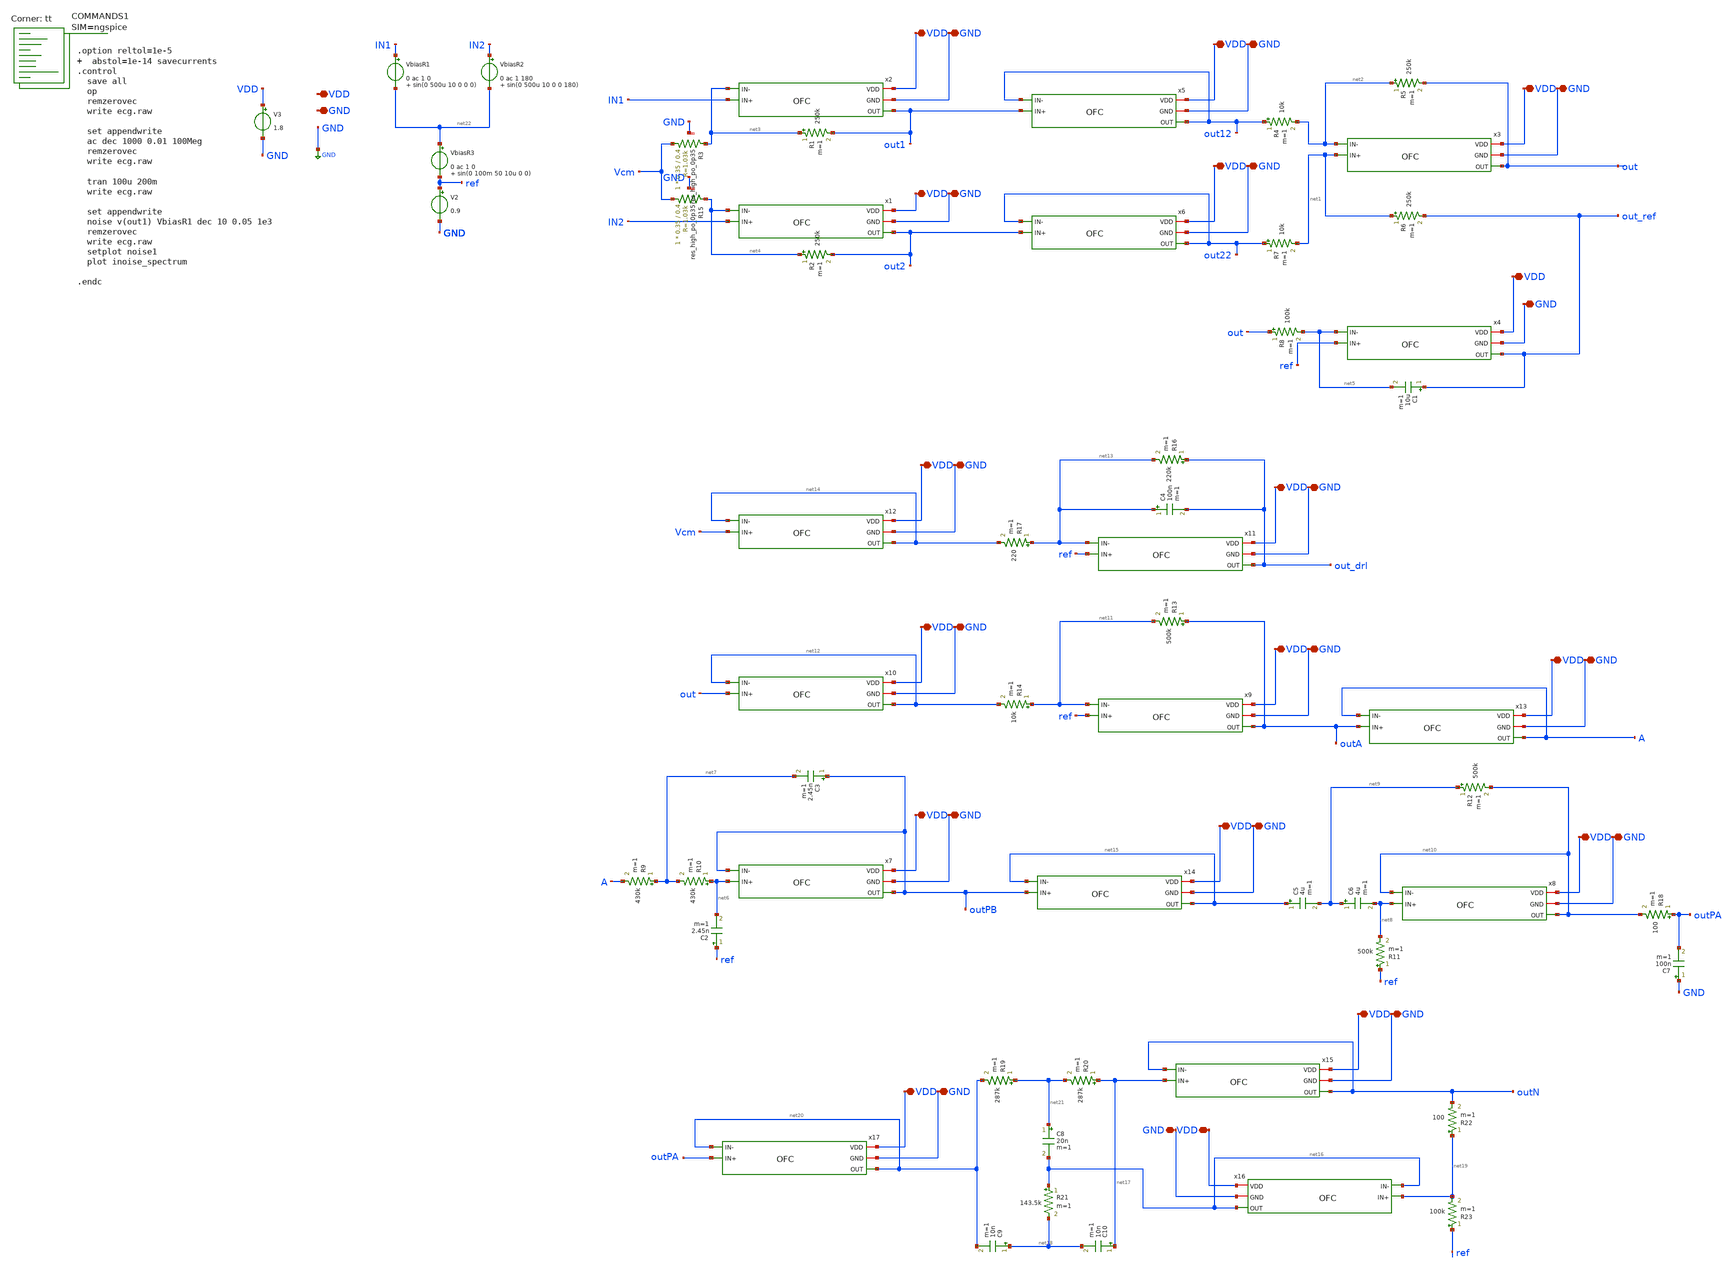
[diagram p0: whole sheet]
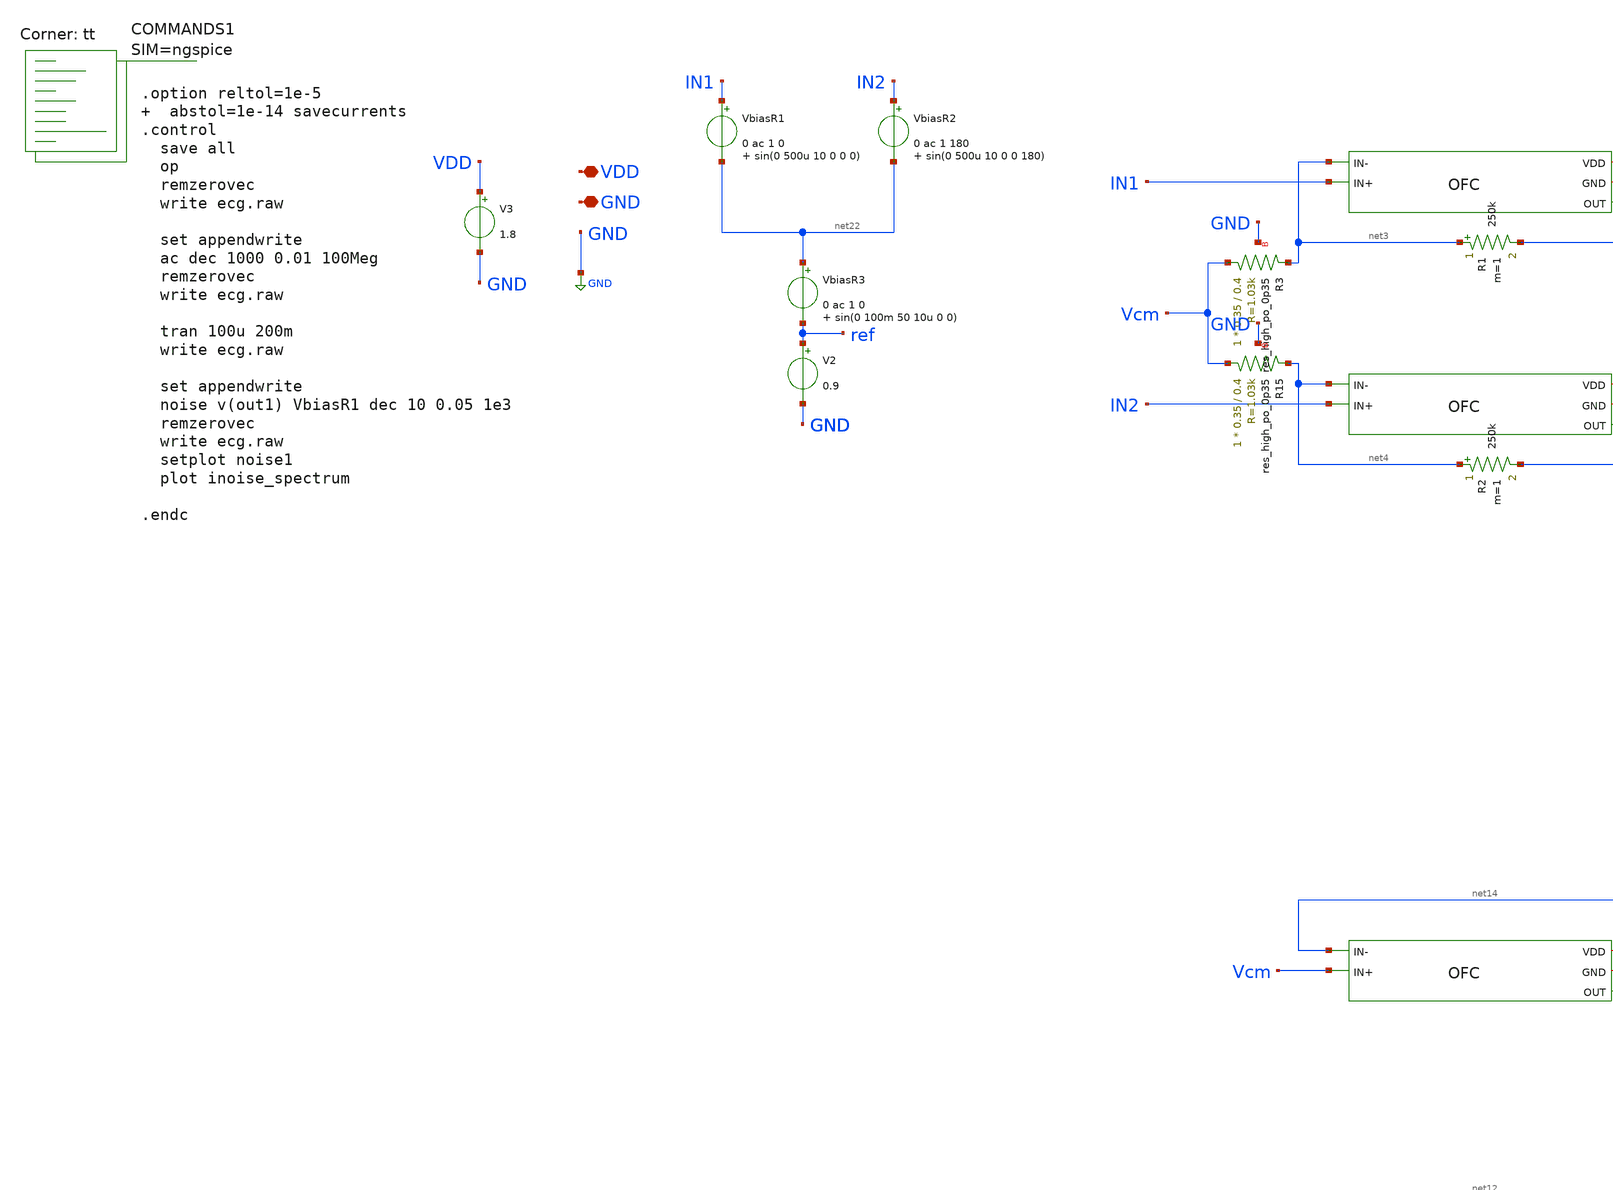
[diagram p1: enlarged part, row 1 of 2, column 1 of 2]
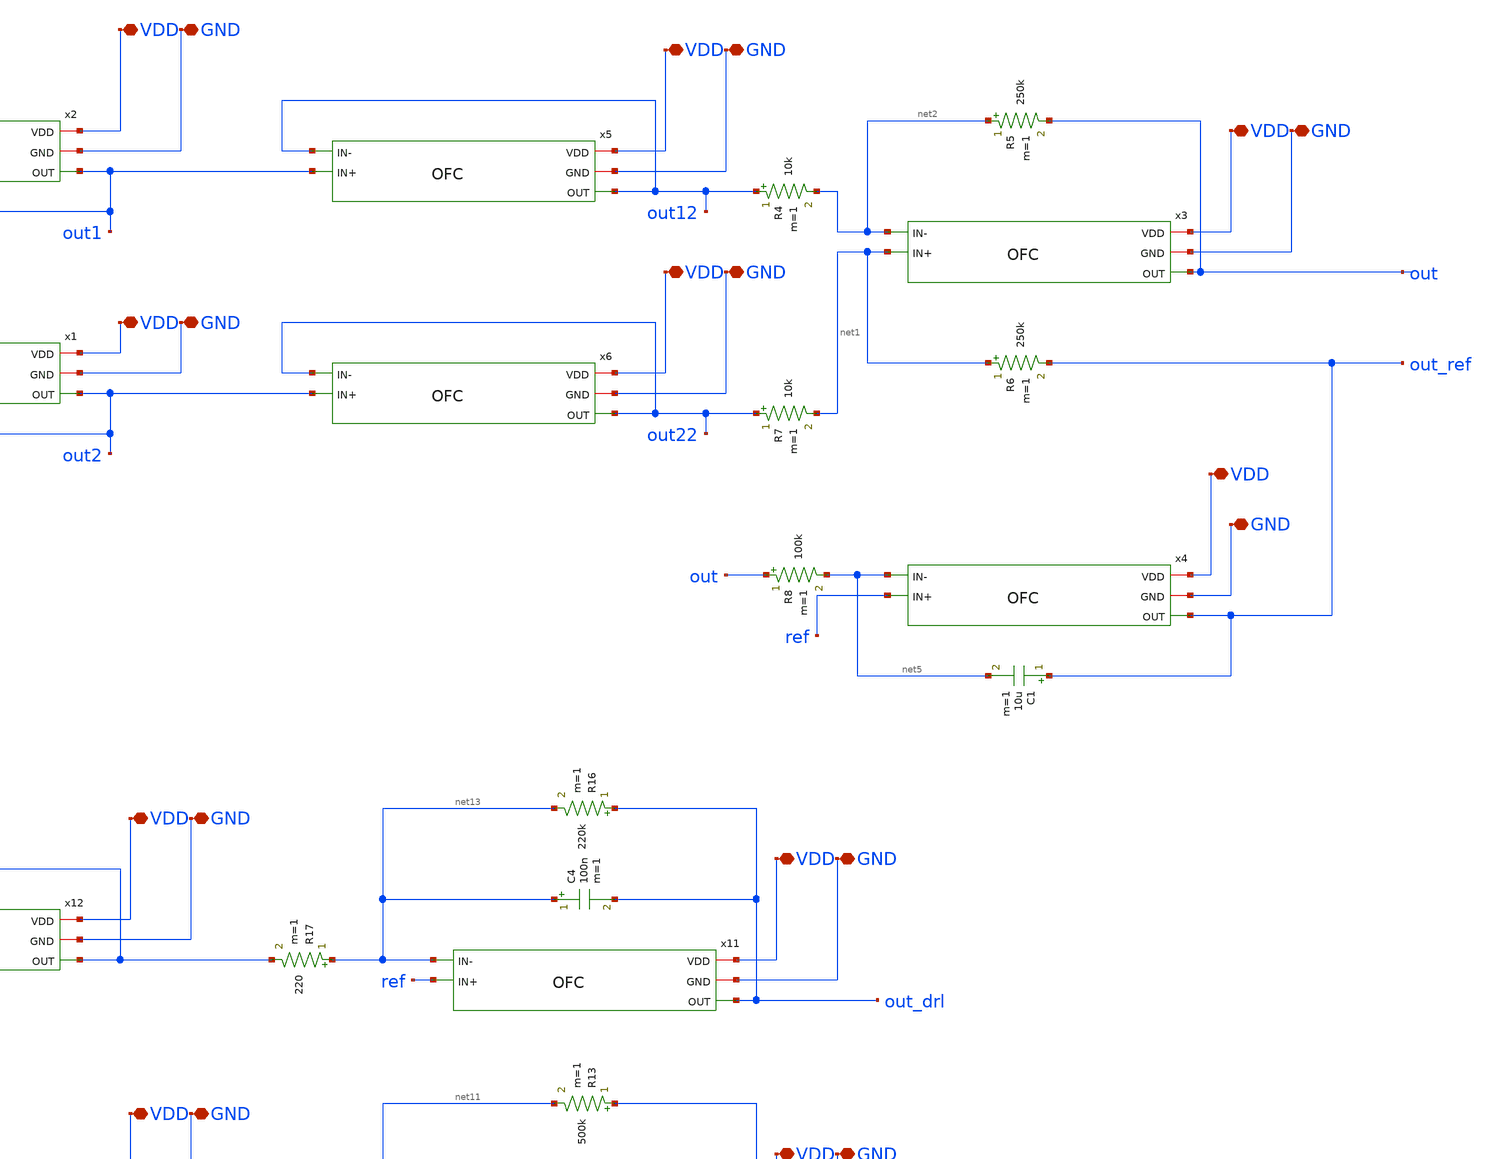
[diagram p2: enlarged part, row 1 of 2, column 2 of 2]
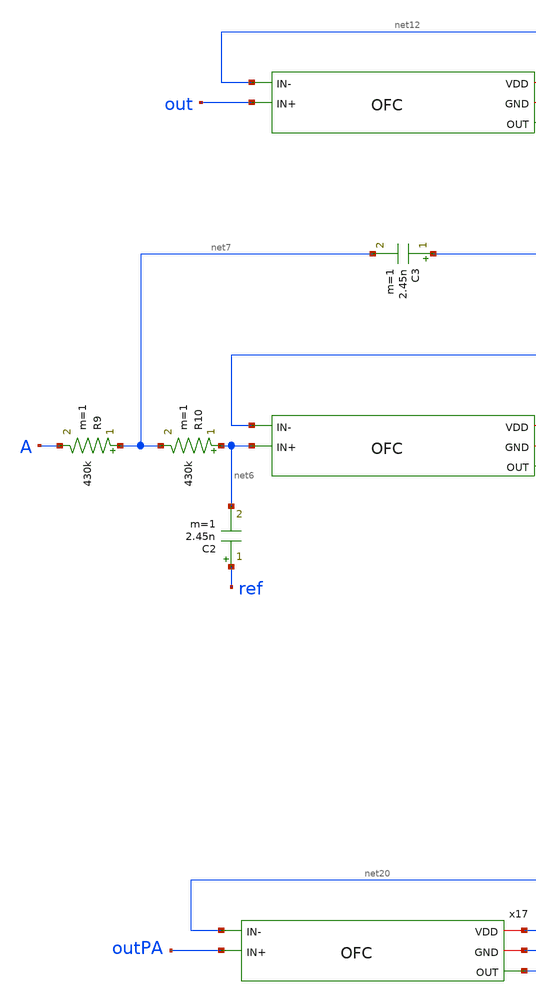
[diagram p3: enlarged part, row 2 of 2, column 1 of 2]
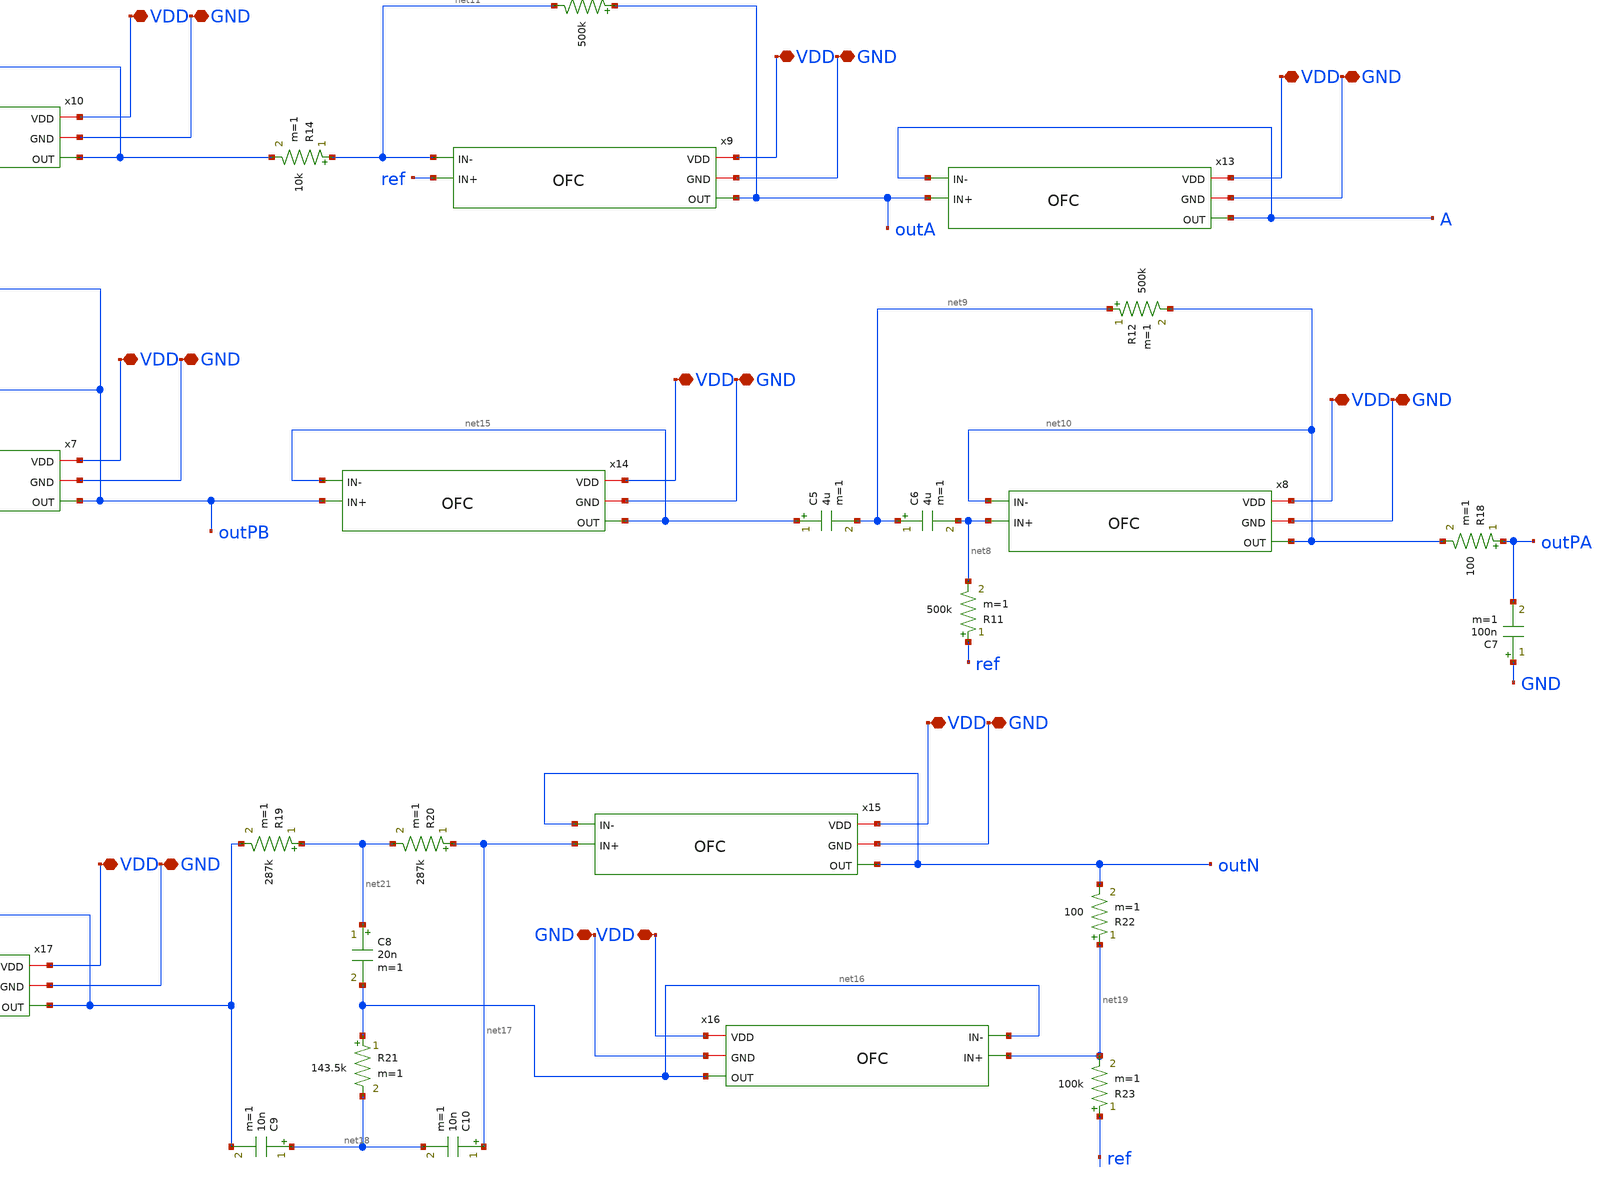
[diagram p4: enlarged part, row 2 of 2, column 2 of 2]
** sch_path: xschem/ecg.sch
**.subckt ecg VDD GND VDD VDD GND GND VDD GND VDD GND VDD GND VDD GND VDD GND VDD GND VDD GND VDD
*+ GND VDD GND VDD GND VDD GND VDD GND VDD GND VDD GND VDD GND
*.iopin VDD
*.iopin GND
*.iopin VDD
*.iopin VDD
*.iopin GND
*.iopin GND
*.iopin VDD
*.iopin GND
*.iopin VDD
*.iopin GND
*.iopin VDD
*.iopin GND
*.iopin VDD
*.iopin GND
*.iopin VDD
*.iopin GND
*.iopin VDD
*.iopin GND
*.iopin VDD
*.iopin GND
*.iopin VDD
*.iopin GND
*.iopin VDD
*.iopin GND
*.iopin VDD
*.iopin GND
*.iopin VDD
*.iopin GND
*.iopin VDD
*.iopin GND
*.iopin VDD
*.iopin GND
*.iopin VDD
*.iopin GND
*.iopin VDD
*.iopin GND
V3 VDD GND 1.8
x1 VDD GND out2 net4 IN2 OFC
x2 VDD GND out1 net3 IN1 OFC
x3 VDD GND out net2 net1 OFC
R1 net3 out1 250k m=1
R2 net4 out2 250k m=1
x4 VDD GND out_ref net5 ref OFC
R6 net1 out_ref 250k m=1
R8 out net5 100k m=1
C1 out_ref net5 10u m=1
R5 net2 out 250k m=1
x5 VDD GND out12 out12 out1 OFC
x6 VDD GND out22 out22 out2 OFC
R4 out12 net2 10k m=1
R7 out22 net1 10k m=1
x7 VDD GND outPB outPB net6 OFC
R9 net7 A 430k m=1
C2 ref net6 2.45n m=1
R10 net6 net7 430k m=1
C3 outPB net7 2.45n m=1
x8 VDD GND net10 net10 net8 OFC
R11 ref net8 500k m=1
C5 net15 net9 4u m=1
C6 net9 net8 4u m=1
x9 VDD GND outA net11 ref OFC
R13 outA net11 500k m=1
R14 net11 net12 10k m=1
x10 VDD GND net12 net12 out OFC
x11 VDD GND out_drl net13 ref OFC
R16 out_drl net13 220k m=1
R17 net13 net14 220 m=1
x12 VDD GND net14 net14 Vcm OFC
C4 net13 out_drl 100n m=1
x13 VDD GND A A outA OFC
x14 VDD GND net15 net15 outPB OFC
C7 GND outPA 100n m=1
R18 outPA net10 100 m=1
R12 net9 net10 500k m=1
XR3 Vcm net3 GND sky130_fd_pr__res_high_po_0p35 L=0.4 mult=1 m=1
XR15 Vcm net4 GND sky130_fd_pr__res_high_po_0p35 L=0.4 mult=1 m=1
x15 VDD GND outN outN net17 OFC
x16 VDD GND net16 net16 net19 OFC
R19 net21 net20 287k m=1
R20 net17 net21 287k m=1
R21 net16 net18 143.5k m=1
C8 net21 net16 20n m=1
C9 net18 net20 10n m=1
C10 net17 net18 10n m=1
R22 net19 outN 100 m=1
R23 ref net19 100k m=1
x17 VDD GND net20 net20 outPA OFC
VbiasR1 IN1 net22 0 ac 1 0 sin(0 500u 10 0 0 0)
V2 ref GND 0.9
VbiasR2 IN2 net22 0 ac 1 180 sin(0 500u 10 0 0 180)
VbiasR3 net22 ref 0 ac 1 0 sin(0 100m 50 10u 0 0)
**** begin user architecture code



.option reltol=1e-5   abstol=1e-14 savecurrents
.control
  save all
  op
  remzerovec
  write ecg.raw

  set appendwrite
  ac dec 1000 0.01 100Meg
  remzerovec
  write ecg.raw

  tran 100u 200m
  write ecg.raw

  set appendwrite
  noise v(out1) VbiasR1 dec 10 0.05 1e3
  remzerovec
  write ecg.raw
  setplot noise1
  plot inoise_spectrum

.endc



.lib $::SKYWATER_MODELS/sky130.lib.spice tt
**** end user architecture code
**.ends

* expanding   symbol:  OFC.sym # of pins=5
** sym_path: OFC.sym
** sch_path: OFC.sch
.subckt OFC VDD GND OUT IN- IN+
*.iopin VDD
*.iopin GND
*.ipin IN+
*.ipin IN-
*.opin OUT
XM11 S Vb VDD VDD sky130_fd_pr__pfet_01v8_lvt L=1 W=60 nf=2 ad='int((nf+1)/2) * W/nf * 0.29' as='int((nf+2)/2) * W/nf * 0.29'
+ pd='2*int((nf+1)/2) * (W/nf + 0.29)' ps='2*int((nf+2)/2) * (W/nf + 0.29)' nrd='0.29 / W' nrs='0.29 / W'
+ sa=0 sb=0 sd=0 mult=2 m=2
XM1 D1 IN+ S S sky130_fd_pr__pfet_01v8_lvt L=10 W=25 nf=2 ad='int((nf+1)/2) * W/nf * 0.29' as='int((nf+2)/2) * W/nf * 0.29'
+ pd='2*int((nf+1)/2) * (W/nf + 0.29)' ps='2*int((nf+2)/2) * (W/nf + 0.29)' nrd='0.29 / W' nrs='0.29 / W'
+ sa=0 sb=0 sd=0 mult=2 m=2
XM2 D2 IN- S S sky130_fd_pr__pfet_01v8_lvt L=10 W=25 nf=2 ad='int((nf+1)/2) * W/nf * 0.29' as='int((nf+2)/2) * W/nf * 0.29'
+ pd='2*int((nf+1)/2) * (W/nf + 0.29)' ps='2*int((nf+2)/2) * (W/nf + 0.29)' nrd='0.29 / W' nrs='0.29 / W'
+ sa=0 sb=0 sd=0 mult=2 m=2
XM3 OUT Vc1 D2 GND sky130_fd_pr__nfet_01v8_lvt L=1 W=4 nf=1 ad='int((nf+1)/2) * W/nf * 0.29' as='int((nf+2)/2) * W/nf * 0.29'
+ pd='2*int((nf+1)/2) * (W/nf + 0.29)' ps='2*int((nf+2)/2) * (W/nf + 0.29)' nrd='0.29 / W' nrs='0.29 / W'
+ sa=0 sb=0 sd=0 mult=1 m=1
XM4 D2 Vc GND GND sky130_fd_pr__nfet_01v8_lvt L=1 W=2.8 nf=1 ad='int((nf+1)/2) * W/nf * 0.29' as='int((nf+2)/2) * W/nf * 0.29'
+ pd='2*int((nf+1)/2) * (W/nf + 0.29)' ps='2*int((nf+2)/2) * (W/nf + 0.29)' nrd='0.29 / W' nrs='0.29 / W'
+ sa=0 sb=0 sd=0 mult=1 m=1
XM5 D1 Vc GND GND sky130_fd_pr__nfet_01v8_lvt L=1 W=2.8 nf=1 ad='int((nf+1)/2) * W/nf * 0.29' as='int((nf+2)/2) * W/nf * 0.29'
+ pd='2*int((nf+1)/2) * (W/nf + 0.29)' ps='2*int((nf+2)/2) * (W/nf + 0.29)' nrd='0.29 / W' nrs='0.29 / W'
+ sa=0 sb=0 sd=0 mult=1 m=1
XM6 G Vc1 D1 GND sky130_fd_pr__nfet_01v8_lvt L=1 W=4 nf=1 ad='int((nf+1)/2) * W/nf * 0.29' as='int((nf+2)/2) * W/nf * 0.29'
+ pd='2*int((nf+1)/2) * (W/nf + 0.29)' ps='2*int((nf+2)/2) * (W/nf + 0.29)' nrd='0.29 / W' nrs='0.29 / W'
+ sa=0 sb=0 sd=0 mult=1 m=1
XM7 G Vc2 D9 D9 sky130_fd_pr__pfet_01v8_lvt L=2.23 W=3 nf=1 ad='int((nf+1)/2) * W/nf * 0.29' as='int((nf+2)/2) * W/nf * 0.29'
+ pd='2*int((nf+1)/2) * (W/nf + 0.29)' ps='2*int((nf+2)/2) * (W/nf + 0.29)' nrd='0.29 / W' nrs='0.29 / W'
+ sa=0 sb=0 sd=0 mult=1 m=1
XM9 D9 G VDD VDD sky130_fd_pr__pfet_01v8_lvt L=2.23 W=4 nf=1 ad='int((nf+1)/2) * W/nf * 0.29' as='int((nf+2)/2) * W/nf * 0.29'
+ pd='2*int((nf+1)/2) * (W/nf + 0.29)' ps='2*int((nf+2)/2) * (W/nf + 0.29)' nrd='0.29 / W' nrs='0.29 / W'
+ sa=0 sb=0 sd=0 mult=1 m=1
XM8 D10 G VDD VDD sky130_fd_pr__pfet_01v8_lvt L=2.23 W=4 nf=1 ad='int((nf+1)/2) * W/nf * 0.29' as='int((nf+2)/2) * W/nf * 0.29'
+ pd='2*int((nf+1)/2) * (W/nf + 0.29)' ps='2*int((nf+2)/2) * (W/nf + 0.29)' nrd='0.29 / W' nrs='0.29 / W'
+ sa=0 sb=0 sd=0 mult=1 m=1
XM10 OUT Vc2 D10 D10 sky130_fd_pr__pfet_01v8_lvt L=2.23 W=3 nf=1 ad='int((nf+1)/2) * W/nf * 0.29' as='int((nf+2)/2) * W/nf * 0.29'
+ pd='2*int((nf+1)/2) * (W/nf + 0.29)' ps='2*int((nf+2)/2) * (W/nf + 0.29)' nrd='0.29 / W' nrs='0.29 / W'
+ sa=0 sb=0 sd=0 mult=1 m=1
XR2 Vb VDD GND sky130_fd_pr__res_xhigh_po_0p35 L=5 mult=1 m=1
XR3 GND Vb GND sky130_fd_pr__res_xhigh_po_0p35 L=13.2 mult=1 m=1
XR1 Vc VDD GND sky130_fd_pr__res_xhigh_po_0p35 L=5 mult=1 m=1
XR4 GND Vc GND sky130_fd_pr__res_xhigh_po_0p35 L=3.07 mult=1 m=1
XR5 Vc1 VDD GND sky130_fd_pr__res_xhigh_po_0p35 L=5 mult=1 m=1
XR6 GND Vc1 GND sky130_fd_pr__res_xhigh_po_0p35 L=13.2 mult=1 m=1
XR7 Vc2 VDD GND sky130_fd_pr__res_xhigh_po_0p35 L=5 mult=1 m=1
XR8 GND Vc2 GND sky130_fd_pr__res_xhigh_po_0p35 L=1.6 mult=1 m=1
.ends

.GLOBAL GND
.end
